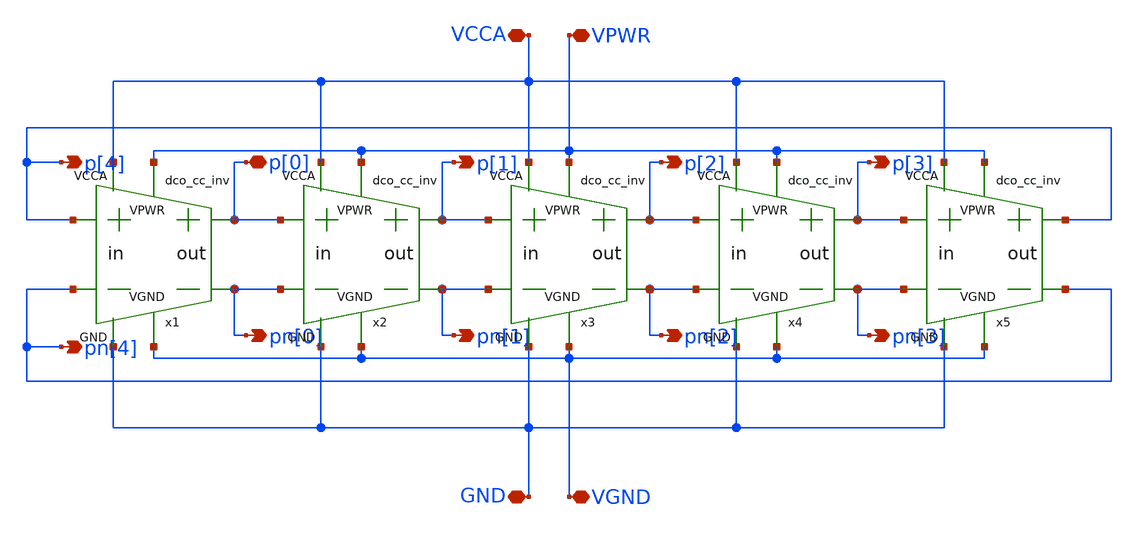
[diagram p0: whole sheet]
** sch_path: xschem/dco_ring_osc.sch
**.subckt dco_ring_osc VPWR VGND pn[0] p[0] pn[1] p[1] p[2] p[3] p[4] pn[2] pn[3] pn[4] VCCA GND
*.iopin VPWR
*.iopin VGND
*.opin pn[0]
*.iopin p[0]
*.opin pn[1]
*.opin p[1]
*.opin p[2]
*.opin p[3]
*.opin p[4]
*.opin pn[2]
*.opin pn[3]
*.opin pn[4]
*.iopin VCCA
*.iopin GND
x1 VCCA VPWR p[0] p[4] pn[4] pn[0] GND VGND dco_cc_inv
x2 VCCA VPWR p[1] p[0] pn[0] pn[1] GND VGND dco_cc_inv
x3 VCCA VPWR p[2] p[1] pn[1] pn[2] GND VGND dco_cc_inv
x4 VCCA VPWR p[3] p[2] pn[2] pn[3] GND VGND dco_cc_inv
x5 VCCA VPWR p[4] p[3] pn[3] pn[4] GND VGND dco_cc_inv
**.ends
.end
